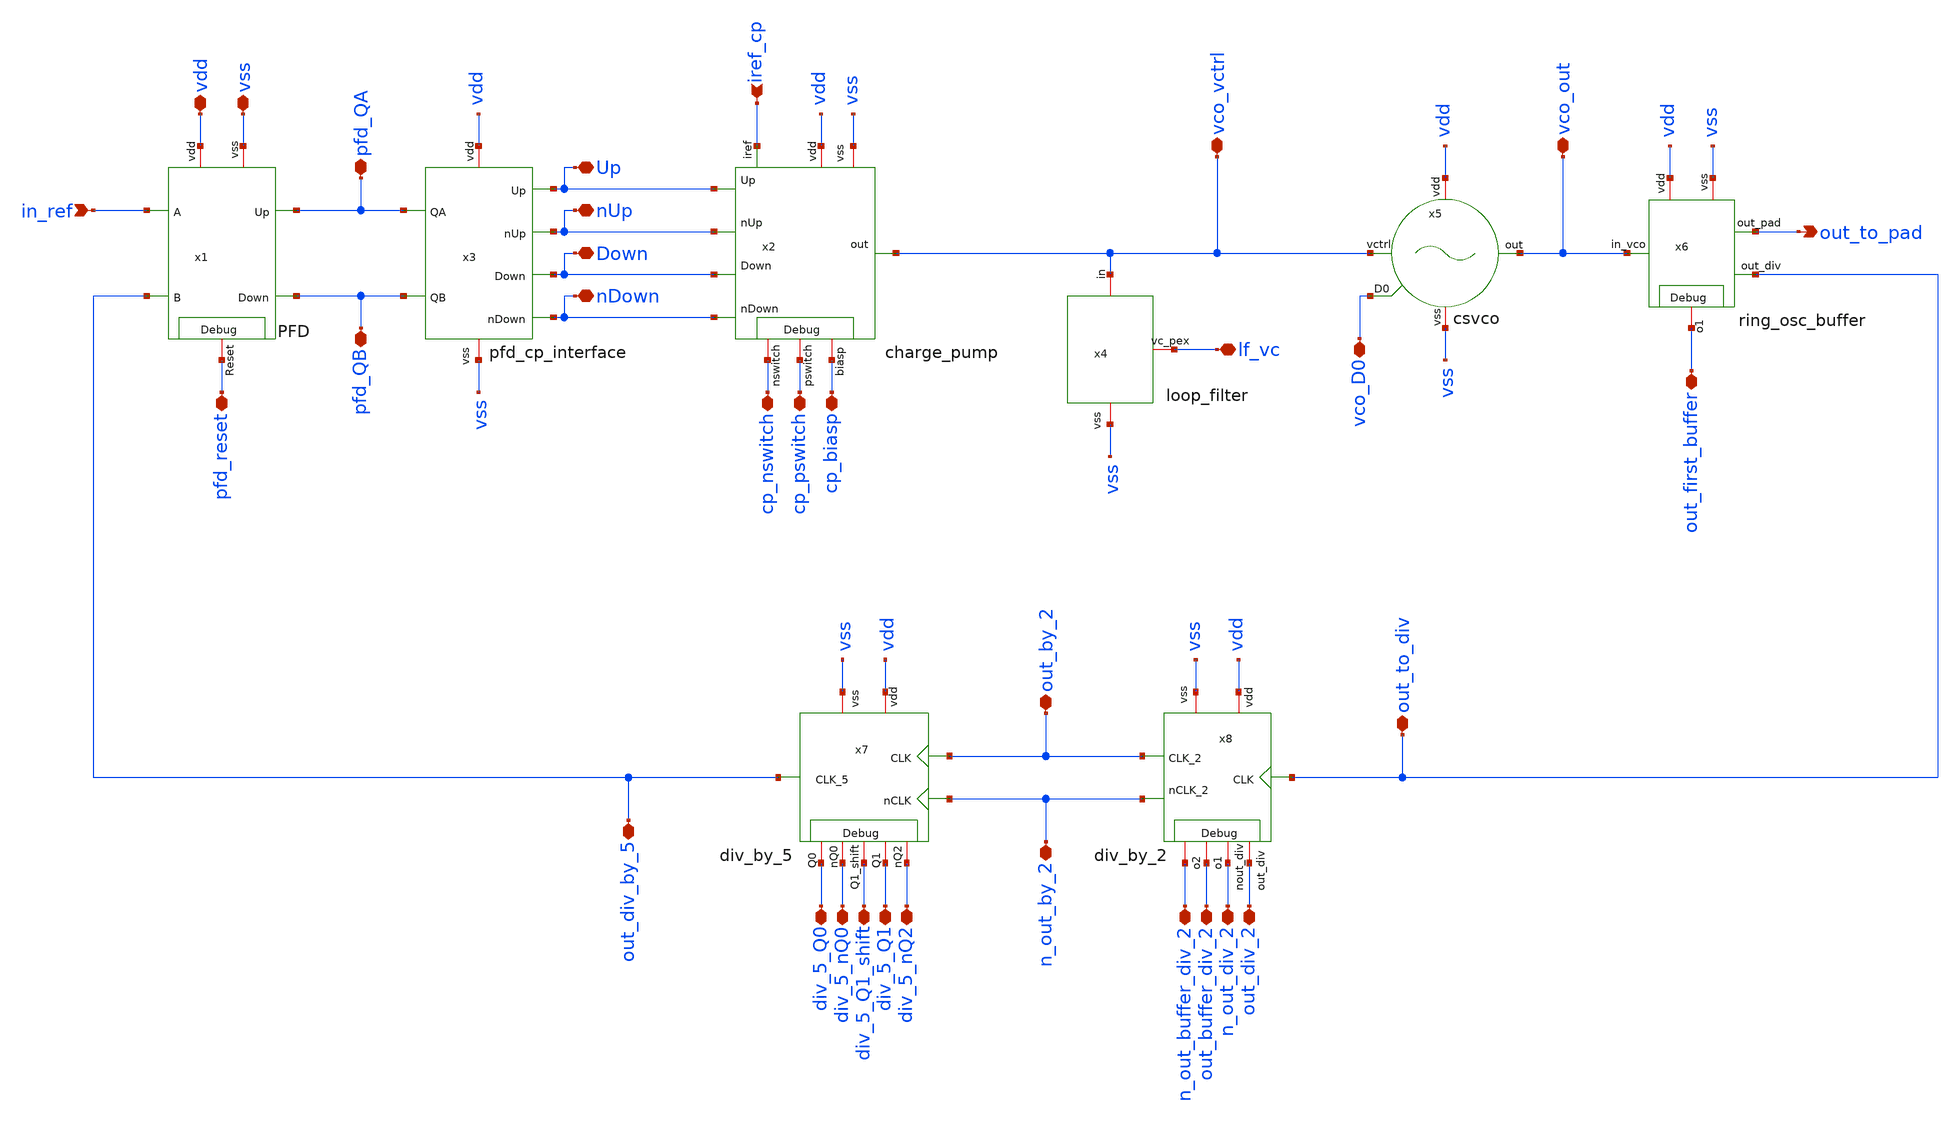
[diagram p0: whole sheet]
** sch_path: xschem/top_pll_v1.sch
**.subckt top_pll_v1 vdd vss in_ref pfd_QA pfd_QB Up nUp Down nDown pfd_reset cp_nswitch cp_pswitch
*+ cp_biasp iref_cp lf_vc vco_D0 vco_vctrl vco_out out_first_buffer out_to_pad out_to_div out_by_2 n_out_by_2
*+ out_div_2 n_out_div_2 out_buffer_div_2 n_out_buffer_div_2 div_5_Q1 div_5_Q1_shift div_5_nQ0 div_5_Q0
*+ div_5_nQ2 out_div_by_5
*.iopin vdd
*.iopin vss
*.ipin in_ref
*.iopin pfd_QA
*.iopin pfd_QB
*.iopin Up
*.iopin nUp
*.iopin Down
*.iopin nDown
*.iopin pfd_reset
*.iopin cp_nswitch
*.iopin cp_pswitch
*.iopin cp_biasp
*.ipin iref_cp
*.iopin lf_vc
*.iopin vco_D0
*.iopin vco_vctrl
*.iopin vco_out
*.iopin out_first_buffer
*.opin out_to_pad
*.iopin out_to_div
*.iopin out_by_2
*.iopin n_out_by_2
*.iopin out_div_2
*.iopin n_out_div_2
*.iopin out_buffer_div_2
*.iopin n_out_buffer_div_2
*.iopin div_5_Q1
*.iopin div_5_Q1_shift
*.iopin div_5_nQ0
*.iopin div_5_Q0
*.iopin div_5_nQ2
*.iopin out_div_by_5
x1 vss vdd pfd_QA in_ref out_div_by_5 pfd_QB pfd_reset PFD
x2 vdd Up nUp vco_vctrl Down nDown vss iref_cp cp_nswitch cp_pswitch cp_biasp charge_pump
x3 Up vdd pfd_QA nUp Down pfd_QB vss nDown pfd_cp_interface
x4 vss vco_vctrl lf_vc loop_filter
x5 vdd vco_out vco_D0 vco_vctrl vss csvco
x6 vdd vco_out out_to_pad out_to_div vss out_first_buffer ring_osc_buffer
x7 vdd out_div_by_5 out_by_2 vss n_out_by_2 div_5_nQ2 div_5_Q1 div_5_nQ0 div_5_Q0 div_5_Q1_shift
+ div_by_5
x8 n_out_by_2 vss out_to_div vdd out_by_2 out_div_2 n_out_div_2 out_buffer_div_2 n_out_buffer_div_2
+ div_by_2
**.ends
.end
